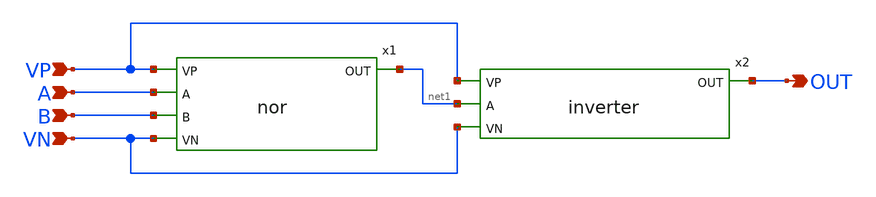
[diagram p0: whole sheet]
** sch_path: basic_cell/or/xschem/or.sch
**.subckt or VP A B VN OUT
*.ipin VP
*.ipin A
*.ipin B
*.ipin VN
*.opin OUT
x1 VP A B net1 VN nor
x2 VP net1 OUT VN inverter
**.ends

* expanding   symbol:  /foss/designs/APIC_Mux_DFF/basic_cell/single_cell/nor/nor.sym # of pins=5
** sym_path: basic_cell/single_cell/nor/nor.sym
** sch_path: basic_cell/single_cell/nor/nor.sch
.subckt nor VP A B OUT VN
*.ipin A
*.ipin B
*.ipin VP
*.ipin VN
*.opin OUT
XM1 OUT A VN VN sky130_fd_pr__nfet_01v8 L=0.15 W=1 nf=1 ad='int((nf+1)/2) * W/nf * 0.29' as='int((nf+2)/2) * W/nf * 0.29'
+ pd='2*int((nf+1)/2) * (W/nf + 0.29)' ps='2*int((nf+2)/2) * (W/nf + 0.29)' nrd='0.29 / W' nrs='0.29 / W'
+ sa=0 sb=0 sd=0 mult=1 m=1
XM2 OUT B VN VN sky130_fd_pr__nfet_01v8 L=0.15 W=1 nf=1 ad='int((nf+1)/2) * W/nf * 0.29' as='int((nf+2)/2) * W/nf * 0.29'
+ pd='2*int((nf+1)/2) * (W/nf + 0.29)' ps='2*int((nf+2)/2) * (W/nf + 0.29)' nrd='0.29 / W' nrs='0.29 / W'
+ sa=0 sb=0 sd=0 mult=1 m=1
XM3 OUT B net1 VP sky130_fd_pr__pfet_01v8 L=0.15 W=3 nf=1 ad='int((nf+1)/2) * W/nf * 0.29' as='int((nf+2)/2) * W/nf * 0.29'
+ pd='2*int((nf+1)/2) * (W/nf + 0.29)' ps='2*int((nf+2)/2) * (W/nf + 0.29)' nrd='0.29 / W' nrs='0.29 / W'
+ sa=0 sb=0 sd=0 mult=1 m=1
XM4 net1 A VP VP sky130_fd_pr__pfet_01v8 L=0.15 W=3 nf=1 ad='int((nf+1)/2) * W/nf * 0.29' as='int((nf+2)/2) * W/nf * 0.29'
+ pd='2*int((nf+1)/2) * (W/nf + 0.29)' ps='2*int((nf+2)/2) * (W/nf + 0.29)' nrd='0.29 / W' nrs='0.29 / W'
+ sa=0 sb=0 sd=0 mult=1 m=1
.ends


* expanding   symbol:  /foss/designs/APIC_Mux_DFF/basic_cell/single_cell/inverter/inverter.sym # of
*+ pins=4
** sym_path: basic_cell/single_cell/inverter/inverter.sym
** sch_path: basic_cell/single_cell/inverter/inverter.sch
.subckt inverter VP A OUT VN
*.ipin A
*.ipin VP
*.ipin VN
*.opin OUT
XM1 OUT A VP VP sky130_fd_pr__pfet_01v8 L=0.15 W=3 nf=1 ad='int((nf+1)/2) * W/nf * 0.29' as='int((nf+2)/2) * W/nf * 0.29'
+ pd='2*int((nf+1)/2) * (W/nf + 0.29)' ps='2*int((nf+2)/2) * (W/nf + 0.29)' nrd='0.29 / W' nrs='0.29 / W'
+ sa=0 sb=0 sd=0 mult=1 m=1
XM2 OUT A VN VN sky130_fd_pr__nfet_01v8 L=0.15 W=1 nf=1 ad='int((nf+1)/2) * W/nf * 0.29' as='int((nf+2)/2) * W/nf * 0.29'
+ pd='2*int((nf+1)/2) * (W/nf + 0.29)' ps='2*int((nf+2)/2) * (W/nf + 0.29)' nrd='0.29 / W' nrs='0.29 / W'
+ sa=0 sb=0 sd=0 mult=1 m=1
.ends

.end
